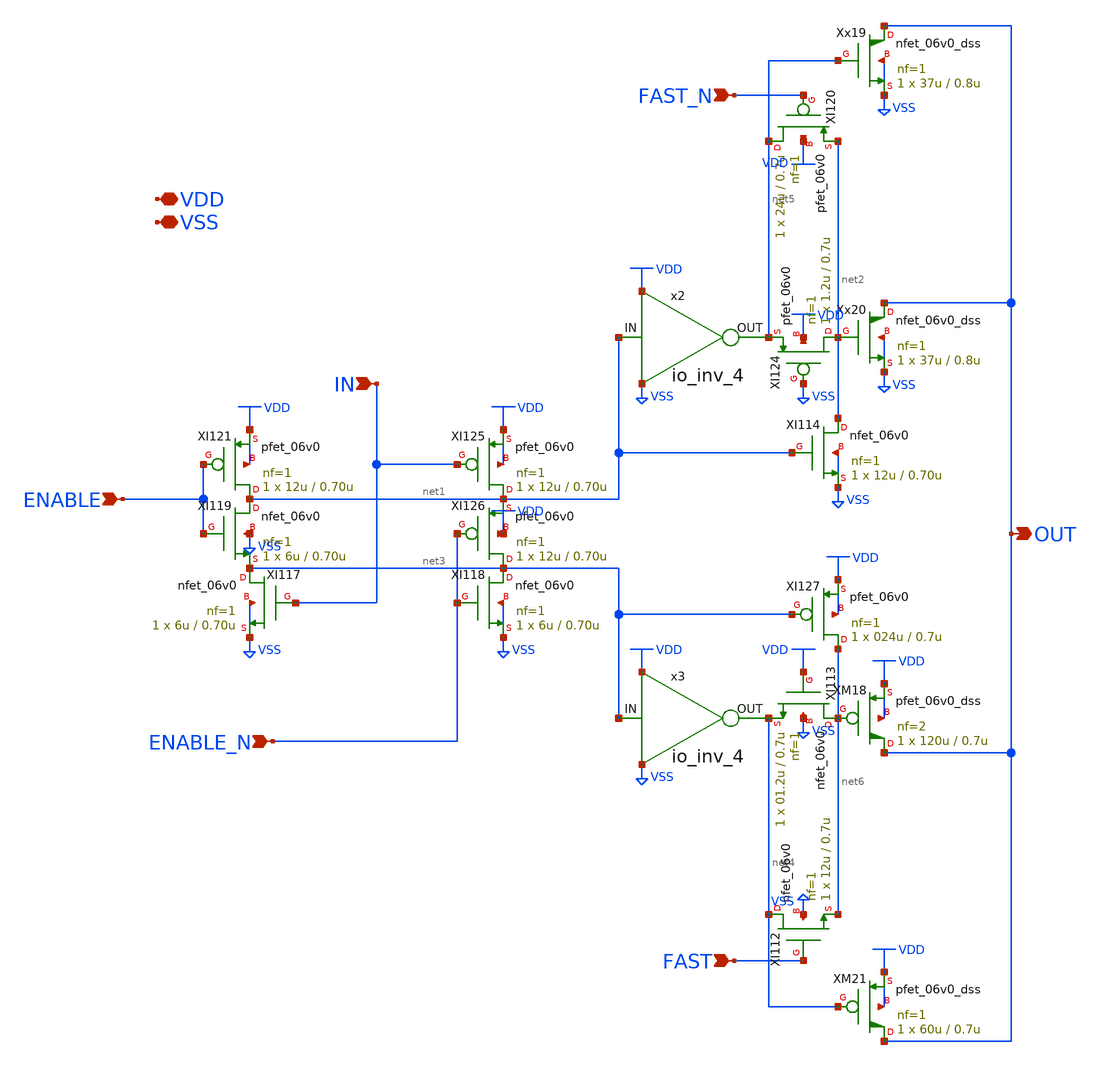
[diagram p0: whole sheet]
** sch_path: xschem/drive_select_24.sch
* Copyright 2023 David Mitchell Bailey
* Licensed under the Apache License, Version 2.0 (the "License");
* you may not use this file except in compliance with the License.
* You may obtain a copy of the License at
* https://www.apache.org/licenses/LICENSE-2.0
* Unless required by applicable law or agreed to in writing, software
* distributed under the License is distributed on an "AS IS" BASIS,
* WITHOUT WARRANTIES OR CONDITIONS OF ANY KIND, either express or implied.
* See the License for the specific language governing permissions and
* limitations under the License.
**.subckt drive_select_24 IN ENABLE FAST FAST_N OUT VDD VSS ENABLE_N
*.ipin IN
*.ipin ENABLE
*.ipin FAST
*.ipin FAST_N
*.opin OUT
*.iopin VDD
*.iopin VSS
*.ipin ENABLE_N
XI121 net1 ENABLE VDD VDD pfet_06v0 L=0.70u W=12u nf=1 ad='int((nf+1)/2) * W/nf * 0.18u' as='int((nf+2)/2) * W/nf * 0.18u'
+ pd='2*int((nf+1)/2) * (W/nf + 0.18u)' ps='2*int((nf+2)/2) * (W/nf + 0.18u)' nrd='0.18u / W' nrs='0.18u / W'
+ sa=0 sb=0 sd=0 m=1
XI125 net1 IN VDD VDD pfet_06v0 L=0.70u W=12u nf=1 ad='int((nf+1)/2) * W/nf * 0.18u' as='int((nf+2)/2) * W/nf * 0.18u'
+ pd='2*int((nf+1)/2) * (W/nf + 0.18u)' ps='2*int((nf+2)/2) * (W/nf + 0.18u)' nrd='0.18u / W' nrs='0.18u / W'
+ sa=0 sb=0 sd=0 m=1
XI126 net3 ENABLE_N net1 VDD pfet_06v0 L=0.70u W=12u nf=1 ad='int((nf+1)/2) * W/nf * 0.18u' as='int((nf+2)/2) * W/nf * 0.18u'
+ pd='2*int((nf+1)/2) * (W/nf + 0.18u)' ps='2*int((nf+2)/2) * (W/nf + 0.18u)' nrd='0.18u / W' nrs='0.18u / W'
+ sa=0 sb=0 sd=0 m=1
XI119 net1 ENABLE net3 VSS nfet_06v0 L=0.70u W=6u nf=1 ad='int((nf+1)/2) * W/nf * 0.18u' as='int((nf+2)/2) * W/nf * 0.18u'
+ pd='2*int((nf+1)/2) * (W/nf + 0.18u)' ps='2*int((nf+2)/2) * (W/nf + 0.18u)' nrd='0.18u / W' nrs='0.18u / W'
+ sa=0 sb=0 sd=0 m=1 par=1
XI117 net3 IN VSS VSS nfet_06v0 L=0.70u W=6u nf=1 ad='int((nf+1)/2) * W/nf * 0.18u' as='int((nf+2)/2) * W/nf * 0.18u'
+ pd='2*int((nf+1)/2) * (W/nf + 0.18u)' ps='2*int((nf+2)/2) * (W/nf + 0.18u)' nrd='0.18u / W' nrs='0.18u / W'
+ sa=0 sb=0 sd=0 m=1 par=1
XI118 net3 ENABLE_N VSS VSS nfet_06v0 L=0.70u W=6u nf=1 ad='int((nf+1)/2) * W/nf * 0.18u' as='int((nf+2)/2) * W/nf * 0.18u'
+ pd='2*int((nf+1)/2) * (W/nf + 0.18u)' ps='2*int((nf+2)/2) * (W/nf + 0.18u)' nrd='0.18u / W' nrs='0.18u / W'
+ sa=0 sb=0 sd=0 m=1 par=1
x2 net1 net5 VDD VSS io_inv_4
XI120 net5 FAST_N net2 VDD pfet_06v0 L=0.7u W=24u nf=1 ad='int((nf+1)/2) * W/nf * 0.18u' as='int((nf+2)/2) * W/nf * 0.18u'
+ pd='2*int((nf+1)/2) * (W/nf + 0.18u)' ps='2*int((nf+2)/2) * (W/nf + 0.18u)' nrd='0.18u / W' nrs='0.18u / W'
+ sa=0 sb=0 sd=0 m=1
Xx20 OUT net2 VSS VSS nfet_06v0_dss L=0.8u W=37u nf=1 ad='int((nf+1)/2) * W/nf * 0.18u' as='int((nf+2)/2) * W/nf * 0.18u'
+ pd='2*int((nf+1)/2) * (W/nf + 0.18u)' ps='2*int((nf+2)/2) * (W/nf + 0.18u)' nrd='0.18u / W' nrs='0.18u / W'
+ sa=0 sb=0 sd=0 d_sab=3.78u s_sab=0.28u m=1
XI114 net2 net1 VSS VSS nfet_06v0 L=0.70u W=12u nf=1 ad='int((nf+1)/2) * W/nf * 0.18u' as='int((nf+2)/2) * W/nf * 0.18u'
+ pd='2*int((nf+1)/2) * (W/nf + 0.18u)' ps='2*int((nf+2)/2) * (W/nf + 0.18u)' nrd='0.18u / W' nrs='0.18u / W'
+ sa=0 sb=0 sd=0 m=1 par=1
XI124 net2 VSS net5 VDD pfet_06v0 L=0.7u W=1.2u nf=1 ad='int((nf+1)/2) * W/nf * 0.18u' as='int((nf+2)/2) * W/nf * 0.18u'
+ pd='2*int((nf+1)/2) * (W/nf + 0.18u)' ps='2*int((nf+2)/2) * (W/nf + 0.18u)' nrd='0.18u / W' nrs='0.18u / W'
+ sa=0 sb=0 sd=0 m=1
Xx19 OUT net5 VSS VSS nfet_06v0_dss L=0.8u W=37u nf=1 ad='int((nf+1)/2) * W/nf * 0.18u' as='int((nf+2)/2) * W/nf * 0.18u'
+ pd='2*int((nf+1)/2) * (W/nf + 0.18u)' ps='2*int((nf+2)/2) * (W/nf + 0.18u)' nrd='0.18u / W' nrs='0.18u / W'
+ sa=0 sb=0 sd=0 d_sab=3.78u s_sab=0.28u m=1
x3 net3 net4 VDD VSS io_inv_4
XI113 net6 VDD net4 VSS nfet_06v0 L=0.7u W=01.2u nf=1 ad='int((nf+1)/2) * W/nf * 0.18u' as='int((nf+2)/2) * W/nf * 0.18u'
+ pd='2*int((nf+1)/2) * (W/nf + 0.18u)' ps='2*int((nf+2)/2) * (W/nf + 0.18u)' nrd='0.18u / W' nrs='0.18u / W'
+ sa=0 sb=0 sd=0 m=1 par=1
XM18 OUT net6 VDD VDD pfet_06v0_dss L=0.7u W=120u nf=2 ad='int((nf+1)/2) * W/nf * 0.18u' as='int((nf+2)/2) * W/nf * 0.18u'
+ pd='2*int((nf+1)/2) * (W/nf + 0.18u)' ps='2*int((nf+2)/2) * (W/nf + 0.18u)' nrd='0.18u / W' nrs='0.18u / W'
+ sa=0 sb=0 sd=0 d_sab=2.78u s_sab=0.28u m=1
XI127 net6 net3 VDD VDD pfet_06v0 L=0.7u W=024u nf=1 ad='int((nf+1)/2) * W/nf * 0.18u' as='int((nf+2)/2) * W/nf * 0.18u'
+ pd='2*int((nf+1)/2) * (W/nf + 0.18u)' ps='2*int((nf+2)/2) * (W/nf + 0.18u)' nrd='0.18u / W' nrs='0.18u / W'
+ sa=0 sb=0 sd=0 m=1
XM21 OUT net4 VDD VDD pfet_06v0_dss L=0.7u W=60u nf=1 ad='int((nf+1)/2) * W/nf * 0.18u' as='int((nf+2)/2) * W/nf * 0.18u'
+ pd='2*int((nf+1)/2) * (W/nf + 0.18u)' ps='2*int((nf+2)/2) * (W/nf + 0.18u)' nrd='0.18u / W' nrs='0.18u / W'
+ sa=0 sb=0 sd=0 d_sab=2.78u s_sab=0.28u m=1
XI112 net4 FAST net6 VSS nfet_06v0 L=0.7u W=12u nf=1 ad='int((nf+1)/2) * W/nf * 0.18u' as='int((nf+2)/2) * W/nf * 0.18u'
+ pd='2*int((nf+1)/2) * (W/nf + 0.18u)' ps='2*int((nf+2)/2) * (W/nf + 0.18u)' nrd='0.18u / W' nrs='0.18u / W'
+ sa=0 sb=0 sd=0 m=1 par=1
**.ends

* expanding   symbol:  io_inv_4.sym # of pins=4
** sym_path: xschem/io_inv_4.sym
** sch_path: xschem/io_inv_4.sch
.subckt io_inv_4 IN OUT VDD VSS
*.opin OUT
*.ipin IN
*.iopin VDD
*.iopin VSS
XM1 OUT IN VDD VDD pfet_06v0 L=0.70u W=24u nf=1 ad='int((nf+1)/2) * W/nf * 0.18u' as='int((nf+2)/2) * W/nf * 0.18u'
+ pd='2*int((nf+1)/2) * (W/nf + 0.18u)' ps='2*int((nf+2)/2) * (W/nf + 0.18u)' nrd='0.18u / W' nrs='0.18u / W'
+ sa=0 sb=0 sd=0 m=1
XM3 OUT IN VSS VSS nfet_06v0 L=0.70u W=12u nf=1 ad='int((nf+1)/2) * W/nf * 0.18u' as='int((nf+2)/2) * W/nf * 0.18u'
+ pd='2*int((nf+1)/2) * (W/nf + 0.18u)' ps='2*int((nf+2)/2) * (W/nf + 0.18u)' nrd='0.18u / W' nrs='0.18u / W'
+ sa=0 sb=0 sd=0 m=1 par=1
.ends

.GLOBAL VDD
.end
